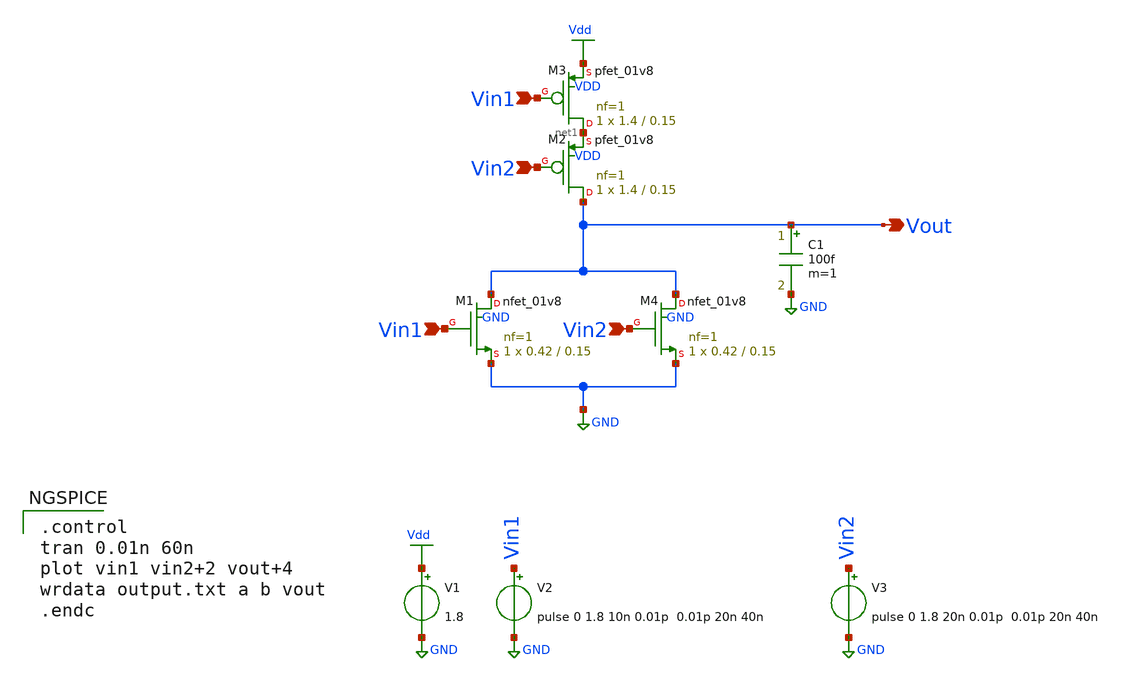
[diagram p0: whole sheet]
** sch_path: Circuiti/porta-nor.sch
**.subckt porta-nor Vout Vin1 Vin1 Vin2 Vin2
*.opin Vout
*.ipin Vin1
*.ipin Vin1
*.ipin Vin2
*.ipin Vin2
XM1 Vout Vin1 GND GND sky130_fd_pr__nfet_01v8 L=0.15 W=0.42 nf=1 ad='int((nf+1)/2) * W/nf * 0.29' as='int((nf+2)/2) * W/nf * 0.29'
+ pd='2*int((nf+1)/2) * (W/nf + 0.29)' ps='2*int((nf+2)/2) * (W/nf + 0.29)' nrd='0.29 / W' nrs='0.29 / W'
+ sa=0 sb=0 sd=0 mult=1 m=1
V1 Vdd GND 1.8
XM2 Vout Vin2 net1 VDD sky130_fd_pr__pfet_01v8 L=0.15 W=1.4 nf=1 ad='int((nf+1)/2) * W/nf * 0.29' as='int((nf+2)/2) * W/nf * 0.29'
+ pd='2*int((nf+1)/2) * (W/nf + 0.29)' ps='2*int((nf+2)/2) * (W/nf + 0.29)' nrd='0.29 / W' nrs='0.29 / W'
+ sa=0 sb=0 sd=0 mult=1 m=1
V2 Vin1 GND pulse 0 1.8 10n 0.01p 0.01p 20n 40n
C1 Vout GND 100f m=1
XM3 net1 Vin1 Vdd VDD sky130_fd_pr__pfet_01v8 L=0.15 W=1.4 nf=1 ad='int((nf+1)/2) * W/nf * 0.29' as='int((nf+2)/2) * W/nf * 0.29'
+ pd='2*int((nf+1)/2) * (W/nf + 0.29)' ps='2*int((nf+2)/2) * (W/nf + 0.29)' nrd='0.29 / W' nrs='0.29 / W'
+ sa=0 sb=0 sd=0 mult=1 m=1
XM4 Vout Vin2 GND GND sky130_fd_pr__nfet_01v8 L=0.15 W=0.42 nf=1 ad='int((nf+1)/2) * W/nf * 0.29' as='int((nf+2)/2) * W/nf * 0.29'
+ pd='2*int((nf+1)/2) * (W/nf + 0.29)' ps='2*int((nf+2)/2) * (W/nf + 0.29)' nrd='0.29 / W' nrs='0.29 / W'
+ sa=0 sb=0 sd=0 mult=1 m=1
V3 Vin2 GND pulse 0 1.8 20n 0.01p 0.01p 20n 40n
**** begin user architecture code


.lib /home/matteo/xschem_downloads/skywater-pdk/libraries/sky130_fd_pr_ngspice/latest/models/sky130.lib.spice tt

*.include /home/matteo/xschem_downloads/skywater-pdk/libraries/sky130_fd_pr_ngspice/latest/cells/nfet_01v8/sky130_fd_pr__nfet_01v8__tt.corner.spice

.param mc_mm_switch=0
.param mc_pr_switch=1



.control
tran 0.01n 60n
plot vin1 vin2+2 vout+4
wrdata output.txt a b vout
.endc


**** end user architecture code
**.ends
.GLOBAL Vdd
.GLOBAL GND
.end
